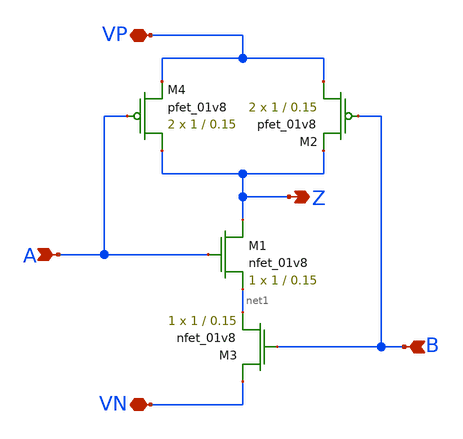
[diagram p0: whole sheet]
** sch_path: schematics/nand.sch
**.subckt nand A VP VN Z B
*.ipin A
*.iopin VP
*.iopin VN
*.opin Z
*.ipin B
XM1 Z A net1 GND sky130_fd_pr__nfet_01v8 L=0.15 W=1 nf=1 ad='int((nf+1)/2) * W/nf * 0.29' as='int((nf+2)/2) * W/nf * 0.29'
+ pd='2*int((nf+1)/2) * (W/nf + 0.29)' ps='2*int((nf+2)/2) * (W/nf + 0.29)' nrd='0.29 / W' nrs='0.29 / W'
+ sa=0 sb=0 sd=0 mult=1 m=1
XM2 VP B Z VDD sky130_fd_pr__pfet_01v8 L=0.15 W=1 nf=1 ad='int((nf+1)/2) * W/nf * 0.29' as='int((nf+2)/2) * W/nf * 0.29'
+ pd='2*int((nf+1)/2) * (W/nf + 0.29)' ps='2*int((nf+2)/2) * (W/nf + 0.29)' nrd='0.29 / W' nrs='0.29 / W'
+ sa=0 sb=0 sd=0 mult=2 m=2
XM3 VN B net1 GND sky130_fd_pr__nfet_01v8 L=0.15 W=1 nf=1 ad='int((nf+1)/2) * W/nf * 0.29' as='int((nf+2)/2) * W/nf * 0.29'
+ pd='2*int((nf+1)/2) * (W/nf + 0.29)' ps='2*int((nf+2)/2) * (W/nf + 0.29)' nrd='0.29 / W' nrs='0.29 / W'
+ sa=0 sb=0 sd=0 mult=1 m=1
XM4 Z A VP VDD sky130_fd_pr__pfet_01v8 L=0.15 W=1 nf=1 ad='int((nf+1)/2) * W/nf * 0.29' as='int((nf+2)/2) * W/nf * 0.29'
+ pd='2*int((nf+1)/2) * (W/nf + 0.29)' ps='2*int((nf+2)/2) * (W/nf + 0.29)' nrd='0.29 / W' nrs='0.29 / W'
+ sa=0 sb=0 sd=0 mult=2 m=2
**.ends
.end
